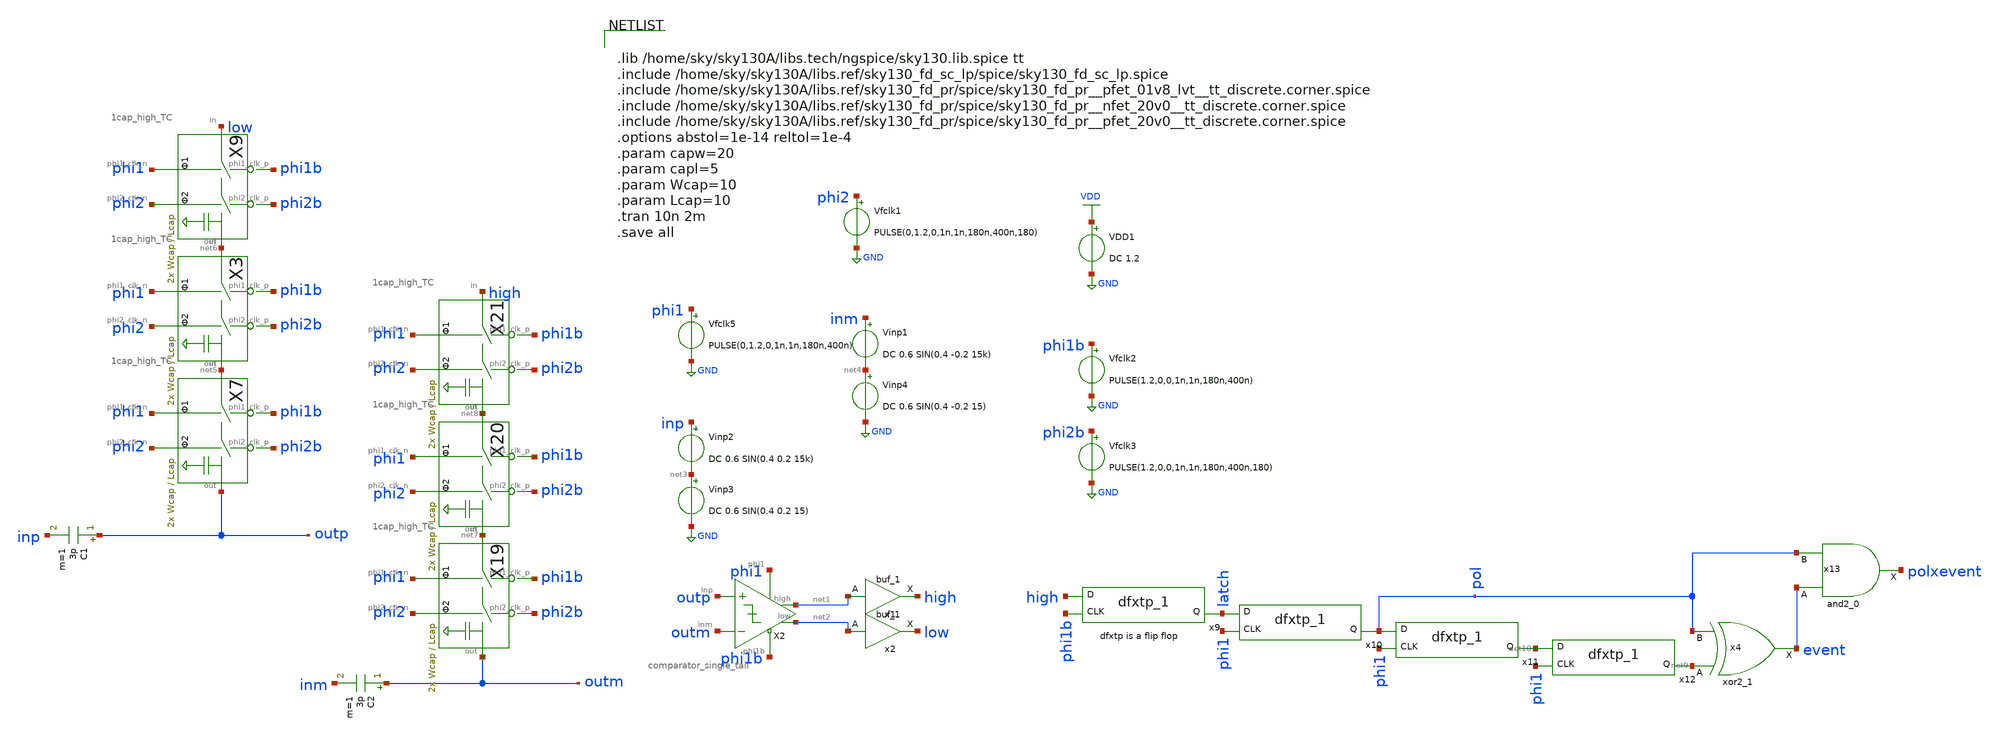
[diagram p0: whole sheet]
** sch_path: xschem/tryandtest/archive/3cao_com_tb_az.sch
**.subckt 3cao_com_tb_az
VDD1 VDD GND DC 1.2
Vfclk5 phi1 GND PULSE(0,1.2,0,1n,1n,180n,400n)
Vfclk1 phi2 GND PULSE(0,1.2,0,1n,1n,180n,400n,180)
Vfclk2 phi1b GND PULSE(1.2,0,0,1n,1n,180n,400n)
Vfclk3 phi2b GND PULSE(1.2,0,0,1n,1n,180n,400n,180)
Vinp2 inp net3 DC 0.6 SIN(0.4 0.2 15k)
Vinp1 inm net4 DC 0.6 SIN(0.4 -0.2 15k)
X7 net5 outp phi2 phi1 phi1b phi2b 1cap_high_TC Wcap=Wcap Lcap=Lcap
X3 net6 net5 phi2 phi1 phi1b phi2b 1cap_high_TC Wcap=Wcap Lcap=Lcap
X9 low net6 phi2 phi1 phi1b phi2b 1cap_high_TC Wcap=Wcap Lcap=Lcap
X2 outp outm net1 phi1 phi1b net2 comparator_single_tail Wplus=0.42 Lplus=0.42 Wminus=0.42
+ Lminus=0.15
X19 net7 outm phi2 phi1 phi1b phi2b 1cap_high_TC Wcap=Wcap Lcap=Lcap
X20 net8 net7 phi2 phi1 phi1b phi2b 1cap_high_TC Wcap=Wcap Lcap=Lcap
X21 high net8 phi2 phi1 phi1b phi2b 1cap_high_TC Wcap=Wcap Lcap=Lcap
x1 net1 GND GND VDD VDD high sky130_fd_sc_lp__buf_1
x2 net2 GND GND VDD VDD low sky130_fd_sc_lp__buf_1
C1 outp inp 3p m=1
C2 outm inm 3p m=1
Vinp3 net3 GND DC 0.6 SIN(0.4 0.2 15)
Vinp4 net4 GND DC 0.6 SIN(0.4 -0.2 15)
x4 net9 pol GND GND VDD VDD event sky130_fd_sc_lp__xor2_1
x11 phi1 pol gnd gnd vdd vdd net10 sky130_fd_sc_lp__dfxtp_1
x12 phi1 net10 gnd gnd vdd vdd net9 sky130_fd_sc_lp__dfxtp_1
x9 phi1b high gnd gnd vdd vdd latch sky130_fd_sc_lp__dfxtp_1
x10 phi1 latch gnd gnd vdd vdd pol sky130_fd_sc_lp__dfxtp_1
x13 event pol GND GND VDD VDD polxevent sky130_fd_sc_lp__and2_0
**** begin user architecture code


.lib /home/sky/sky130A/libs.tech/ngspice/sky130.lib.spice tt
.include /home/sky/sky130A/libs.ref/sky130_fd_sc_lp/spice/sky130_fd_sc_lp.spice
.include /home/sky/sky130A/libs.ref/sky130_fd_pr/spice/sky130_fd_pr__pfet_01v8_lvt__tt_discrete.corner.spice
.include /home/sky/sky130A/libs.ref/sky130_fd_pr/spice/sky130_fd_pr__nfet_20v0__tt_discrete.corner.spice
.include /home/sky/sky130A/libs.ref/sky130_fd_pr/spice/sky130_fd_pr__pfet_20v0__tt_discrete.corner.spice
.options abstol=1e-14 reltol=1e-4
.param capw=20
.param capl=5
.param Wcap=10
.param Lcap=10
.tran 10n 2m
.save all


**** end user architecture code
**.ends
.GLOBAL GND
.GLOBAL VDD
.end
